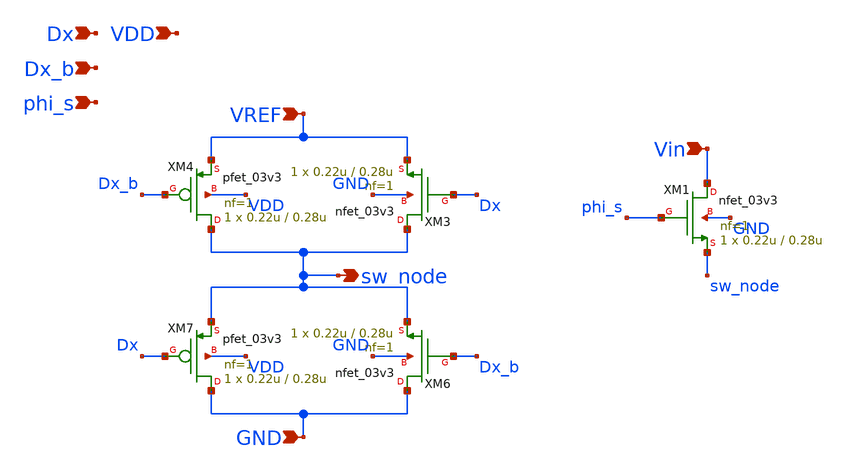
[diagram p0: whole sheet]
** sch_path: analog/blocks/cdac/transistors2.sch
**.subckt transistors2 Vin VREF sw_node GND Dx Dx_b phi_s VDD
*.ipin Vin
*.ipin VREF
*.opin sw_node
*.ipin GND
*.ipin Dx
*.ipin Dx_b
*.ipin phi_s
*.ipin VDD
XM3 sw_node Dx VREF GND nfet_03v3 L=0.28u W=0.22u nf=1 ad='int((nf+1)/2) * W/nf * 0.18u' as='int((nf+2)/2) * W/nf * 0.18u'
+ pd='2*int((nf+1)/2) * (W/nf + 0.18u)' ps='2*int((nf+2)/2) * (W/nf + 0.18u)' nrd='0.18u / W' nrs='0.18u / W'
+ sa=0 sb=0 sd=0 m=1
XM4 sw_node Dx_b VREF VDD pfet_03v3 L=0.28u W=0.22u nf=1 ad='int((nf+1)/2) * W/nf * 0.18u' as='int((nf+2)/2) * W/nf * 0.18u'
+ pd='2*int((nf+1)/2) * (W/nf + 0.18u)' ps='2*int((nf+2)/2) * (W/nf + 0.18u)' nrd='0.18u / W' nrs='0.18u / W'
+ sa=0 sb=0 sd=0 m=1
XM6 GND Dx_b sw_node GND nfet_03v3 L=0.28u W=0.22u nf=1 ad='int((nf+1)/2) * W/nf * 0.18u' as='int((nf+2)/2) * W/nf * 0.18u'
+ pd='2*int((nf+1)/2) * (W/nf + 0.18u)' ps='2*int((nf+2)/2) * (W/nf + 0.18u)' nrd='0.18u / W' nrs='0.18u / W'
+ sa=0 sb=0 sd=0 m=1
XM7 GND Dx sw_node VDD pfet_03v3 L=0.28u W=0.22u nf=1 ad='int((nf+1)/2) * W/nf * 0.18u' as='int((nf+2)/2) * W/nf * 0.18u'
+ pd='2*int((nf+1)/2) * (W/nf + 0.18u)' ps='2*int((nf+2)/2) * (W/nf + 0.18u)' nrd='0.18u / W' nrs='0.18u / W'
+ sa=0 sb=0 sd=0 m=1
XM1 Vin phi_s sw_node GND nfet_03v3 L=0.28u W=0.22u nf=1 ad='int((nf+1)/2) * W/nf * 0.18u' as='int((nf+2)/2) * W/nf * 0.18u'
+ pd='2*int((nf+1)/2) * (W/nf + 0.18u)' ps='2*int((nf+2)/2) * (W/nf + 0.18u)' nrd='0.18u / W' nrs='0.18u / W'
+ sa=0 sb=0 sd=0 m=1
**.ends
.end
